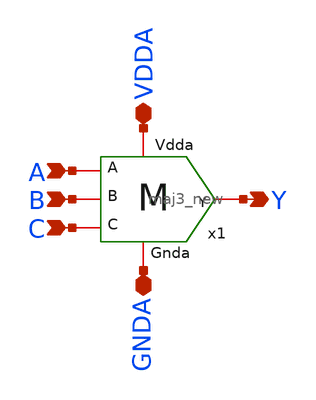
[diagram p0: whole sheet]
** sch_path: xschem/gf180mcu_osu_sc_gp9t3v3__maj3_sim.sch
**.subckt gf180mcu_osu_sc_gp9t3v3__maj3_sim A B C Y VDDA GNDA
*.ipin A
*.ipin B
*.ipin C
*.opin Y
*.iopin VDDA
*.iopin GNDA
x1 VDDA A Y B C GNDA maj3_new
**** begin user architecture code

.lib /foss/pdks/gf180mcuD/libs.tech/ngspice/sm141064.ngspice typical
.param fnoicor=1
.param sw_stat_mismatch=0
V1 VDDA GND 3.3
V2 GNDA GND 0
V3 A GND PULSE(0 3.3 10n 100p 100p 10n 20n)
V4 B GND PULSE(0 3.3 0 100p 100p 20n 40n)
V5 C GND PULSE(0 3.3 0 100p 100p 40n 80n)
.tran 10p 100n
.control
set filetype=ascii
run
write simulate.raw
plot v(A)-7 v(B)-3.5 v(C) v(Y)+3.5
.endc

**** end user architecture code
**.ends

* expanding   symbol:  maj3_new.sym # of pins=6
** sym_path: xschem/maj3_new.sym
** sch_path: xschem/maj3_new.sch
.subckt maj3_new Vdda A Y B C Gnda
*.iopin Vdda
*.iopin Gnda
*.iopin A
*.iopin B
*.iopin C
*.iopin Y
XM1 net1 A Vdda Vdda pfet_03v3 L=0.28u W=0.22u nf=1 ad='int((nf+1)/2) * W/nf * 0.18u' as='int((nf+2)/2) * W/nf * 0.18u'
+ pd='2*int((nf+1)/2) * (W/nf + 0.18u)' ps='2*int((nf+2)/2) * (W/nf + 0.18u)' nrd='0.18u / W' nrs='0.18u / W'
+ sa=0 sb=0 sd=0 m=1
XM2 X C net1 Vdda pfet_03v3 L=0.28u W=0.22u nf=1 ad='int((nf+1)/2) * W/nf * 0.18u' as='int((nf+2)/2) * W/nf * 0.18u'
+ pd='2*int((nf+1)/2) * (W/nf + 0.18u)' ps='2*int((nf+2)/2) * (W/nf + 0.18u)' nrd='0.18u / W' nrs='0.18u / W'
+ sa=0 sb=0 sd=0 m=1
XM3 net6 B Vdda Vdda pfet_03v3 L=0.28u W=0.22u nf=1 ad='int((nf+1)/2) * W/nf * 0.18u' as='int((nf+2)/2) * W/nf * 0.18u'
+ pd='2*int((nf+1)/2) * (W/nf + 0.18u)' ps='2*int((nf+2)/2) * (W/nf + 0.18u)' nrd='0.18u / W' nrs='0.18u / W'
+ sa=0 sb=0 sd=0 m=1
XM5 net2 B Vdda Vdda pfet_03v3 L=0.28u W=0.22u nf=1 ad='int((nf+1)/2) * W/nf * 0.18u' as='int((nf+2)/2) * W/nf * 0.18u'
+ pd='2*int((nf+1)/2) * (W/nf + 0.18u)' ps='2*int((nf+2)/2) * (W/nf + 0.18u)' nrd='0.18u / W' nrs='0.18u / W'
+ sa=0 sb=0 sd=0 m=1
XM6 X A net2 Vdda pfet_03v3 L=0.28u W=0.22u nf=1 ad='int((nf+1)/2) * W/nf * 0.18u' as='int((nf+2)/2) * W/nf * 0.18u'
+ pd='2*int((nf+1)/2) * (W/nf + 0.18u)' ps='2*int((nf+2)/2) * (W/nf + 0.18u)' nrd='0.18u / W' nrs='0.18u / W'
+ sa=0 sb=0 sd=0 m=1
XM4 X C net6 Vdda pfet_03v3 L=0.28u W=0.22u nf=1 ad='int((nf+1)/2) * W/nf * 0.18u' as='int((nf+2)/2) * W/nf * 0.18u'
+ pd='2*int((nf+1)/2) * (W/nf + 0.18u)' ps='2*int((nf+2)/2) * (W/nf + 0.18u)' nrd='0.18u / W' nrs='0.18u / W'
+ sa=0 sb=0 sd=0 m=1
XM7 X C net5 Gnda nfet_03v3 L=0.28u W=0.22u nf=1 ad='int((nf+1)/2) * W/nf * 0.18u' as='int((nf+2)/2) * W/nf * 0.18u'
+ pd='2*int((nf+1)/2) * (W/nf + 0.18u)' ps='2*int((nf+2)/2) * (W/nf + 0.18u)' nrd='0.18u / W' nrs='0.18u / W'
+ sa=0 sb=0 sd=0 m=1
XM8 net5 A Gnda Gnda nfet_03v3 L=0.28u W=0.22u nf=1 ad='int((nf+1)/2) * W/nf * 0.18u' as='int((nf+2)/2) * W/nf * 0.18u'
+ pd='2*int((nf+1)/2) * (W/nf + 0.18u)' ps='2*int((nf+2)/2) * (W/nf + 0.18u)' nrd='0.18u / W' nrs='0.18u / W'
+ sa=0 sb=0 sd=0 m=1
XM9 X C net4 Gnda nfet_03v3 L=0.28u W=0.22u nf=1 ad='int((nf+1)/2) * W/nf * 0.18u' as='int((nf+2)/2) * W/nf * 0.18u'
+ pd='2*int((nf+1)/2) * (W/nf + 0.18u)' ps='2*int((nf+2)/2) * (W/nf + 0.18u)' nrd='0.18u / W' nrs='0.18u / W'
+ sa=0 sb=0 sd=0 m=1
XM10 net4 B Gnda Gnda nfet_03v3 L=0.28u W=0.22u nf=1 ad='int((nf+1)/2) * W/nf * 0.18u' as='int((nf+2)/2) * W/nf * 0.18u'
+ pd='2*int((nf+1)/2) * (W/nf + 0.18u)' ps='2*int((nf+2)/2) * (W/nf + 0.18u)' nrd='0.18u / W' nrs='0.18u / W'
+ sa=0 sb=0 sd=0 m=1
XM11 X A net3 Gnda nfet_03v3 L=0.28u W=0.22u nf=1 ad='int((nf+1)/2) * W/nf * 0.18u' as='int((nf+2)/2) * W/nf * 0.18u'
+ pd='2*int((nf+1)/2) * (W/nf + 0.18u)' ps='2*int((nf+2)/2) * (W/nf + 0.18u)' nrd='0.18u / W' nrs='0.18u / W'
+ sa=0 sb=0 sd=0 m=1
XM12 net3 B Gnda Gnda nfet_03v3 L=0.28u W=0.22u nf=1 ad='int((nf+1)/2) * W/nf * 0.18u' as='int((nf+2)/2) * W/nf * 0.18u'
+ pd='2*int((nf+1)/2) * (W/nf + 0.18u)' ps='2*int((nf+2)/2) * (W/nf + 0.18u)' nrd='0.18u / W' nrs='0.18u / W'
+ sa=0 sb=0 sd=0 m=1
XM13 Y X Vdda Vdda pfet_03v3 L=0.28u W=0.22u nf=1 ad='int((nf+1)/2) * W/nf * 0.18u' as='int((nf+2)/2) * W/nf * 0.18u'
+ pd='2*int((nf+1)/2) * (W/nf + 0.18u)' ps='2*int((nf+2)/2) * (W/nf + 0.18u)' nrd='0.18u / W' nrs='0.18u / W'
+ sa=0 sb=0 sd=0 m=1
XM14 Y X Vdda Vdda pfet_03v3 L=0.28u W=0.22u nf=1 ad='int((nf+1)/2) * W/nf * 0.18u' as='int((nf+2)/2) * W/nf * 0.18u'
+ pd='2*int((nf+1)/2) * (W/nf + 0.18u)' ps='2*int((nf+2)/2) * (W/nf + 0.18u)' nrd='0.18u / W' nrs='0.18u / W'
+ sa=0 sb=0 sd=0 m=1
XM15 Y X Gnda Gnda nfet_03v3 L=0.28u W=0.22u nf=1 ad='int((nf+1)/2) * W/nf * 0.18u' as='int((nf+2)/2) * W/nf * 0.18u'
+ pd='2*int((nf+1)/2) * (W/nf + 0.18u)' ps='2*int((nf+2)/2) * (W/nf + 0.18u)' nrd='0.18u / W' nrs='0.18u / W'
+ sa=0 sb=0 sd=0 m=1
XM16 Y X Gnda Gnda nfet_03v3 L=0.28u W=0.22u nf=1 ad='int((nf+1)/2) * W/nf * 0.18u' as='int((nf+2)/2) * W/nf * 0.18u'
+ pd='2*int((nf+1)/2) * (W/nf + 0.18u)' ps='2*int((nf+2)/2) * (W/nf + 0.18u)' nrd='0.18u / W' nrs='0.18u / W'
+ sa=0 sb=0 sd=0 m=1
**** begin user architecture code
B
**** end user architecture code
.ends

.end
